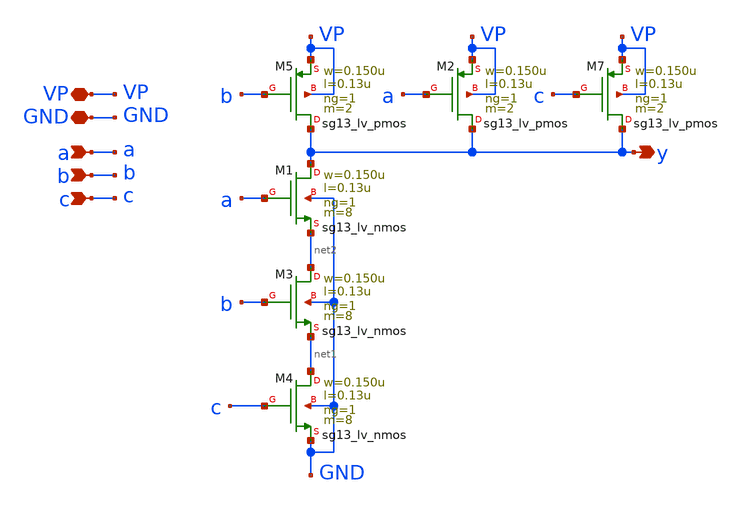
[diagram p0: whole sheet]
** sch_path: schematics/divider/schematics/NAND_3in_x2.sch
**.subckt NAND_3in_x2 y GND a VP b c
*.opin y
*.iopin GND
*.ipin a
*.iopin VP
*.ipin b
*.ipin c
XM1 y a net2 GND sg13_lv_nmos w=0.150u l=0.13u ng=1 m=8 mm_ok=1
XM3 net2 b net1 GND sg13_lv_nmos w=0.150u l=0.13u ng=1 m=8 mm_ok=1
XM4 net1 c GND GND sg13_lv_nmos w=0.150u l=0.13u ng=1 m=8 mm_ok=1
XM7 y c VP VP sg13_lv_pmos w=0.150u l=0.13u ng=1 m=2 mm_ok=1
XM2 y a VP VP sg13_lv_pmos w=0.150u l=0.13u ng=1 m=2 mm_ok=1
XM5 y b VP VP sg13_lv_pmos w=0.150u l=0.13u ng=1 m=2 mm_ok=1
**.ends
.end
